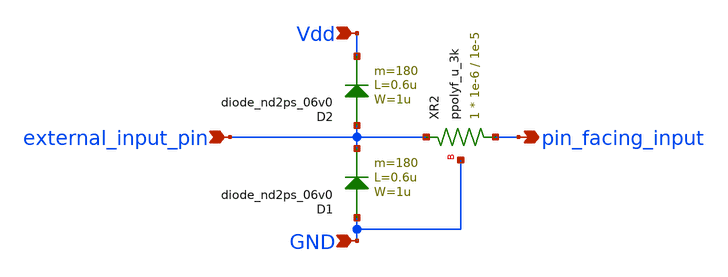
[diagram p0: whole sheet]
** sch_path: MG_ESD_protection/MG_ESD_protection.sch
**.subckt MG_ESD_protection external_input_pin Vdd GND pin_facing_input
*.ipin external_input_pin
*.ipin Vdd
*.ipin GND
*.opin pin_facing_input
D2 external_input_pin Vdd diode_nd2ps_06v0 area='1u * 0.6u ' pj='2*1u + 2*0.6u ' m=180
XR2 pin_facing_input external_input_pin GND ppolyf_u_3k r_width=1e-6 r_length=1e-5 m=1
D1 GND external_input_pin diode_nd2ps_06v0 area='1u * 0.6u ' pj='2*1u + 2*0.6u ' m=180
**.ends
.end
